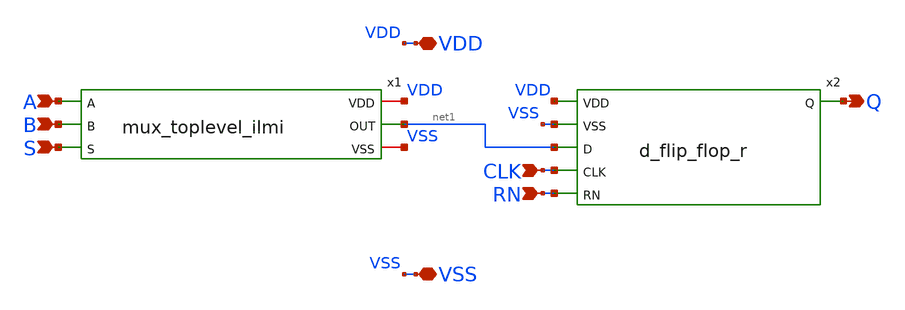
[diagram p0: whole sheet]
** sch_path: designs/libs/sdffrq_tg_toplevel_ilmi/sdffrq_var_tg_toplevel.sch
**.subckt sdffrq_var_tg_toplevel A B S VDD VSS Q RN CLK
*.ipin A
*.ipin B
*.ipin S
*.iopin VDD
*.iopin VSS
*.opin Q
*.ipin RN
*.ipin CLK
x2 VDD VSS Q net1 CLK RN d_flip_flop_r
x1 VDD A net1 B VSS S mux_toplevel_ilmi
**.ends
.end
